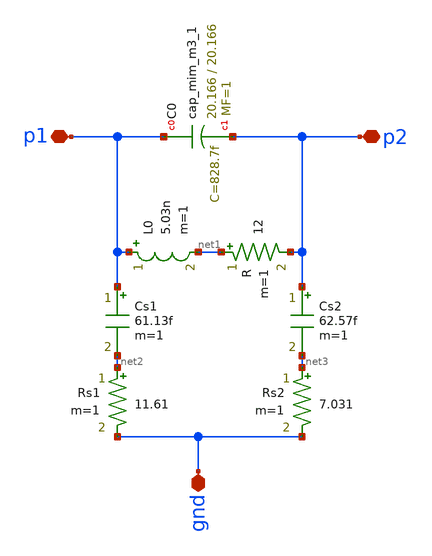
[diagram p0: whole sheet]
** sch_path: xschem/lc.sch
**.subckt lc p1 p2 gnd
*.iopin p1
*.iopin p2
*.iopin gnd
L0 p1 net1 5.03n m=1
XC0 p1 p2 sky130_fd_pr__cap_mim_m3_1 W=20.166 L=20.166 MF=1 m=1
R net1 p2 12 m=1
Cs2 p2 net3 62.57f m=1
Cs1 p1 net2 61.13f m=1
Rs1 net2 gnd 11.61 m=1
Rs2 net3 gnd 7.031 m=1
**.ends
.end
